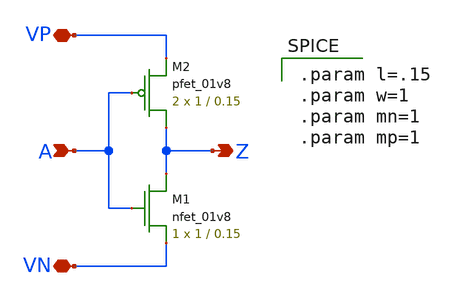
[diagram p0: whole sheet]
** sch_path: schematics/inverter.sch
**.subckt inverter A VP VN Z
*.ipin A
*.iopin VP
*.iopin VN
*.opin Z
XM1 Z A VN GND sky130_fd_pr__nfet_01v8 L=0.15 W=1 nf=1 ad='int((nf+1)/2) * W/nf * 0.29' as='int((nf+2)/2) * W/nf * 0.29'
+ pd='2*int((nf+1)/2) * (W/nf + 0.29)' ps='2*int((nf+2)/2) * (W/nf + 0.29)' nrd='0.29 / W' nrs='0.29 / W'
+ sa=0 sb=0 sd=0 mult=1 m=1
XM2 Z A VP VDD sky130_fd_pr__pfet_01v8 L=0.15 W=1 nf=1 ad='int((nf+1)/2) * W/nf * 0.29' as='int((nf+2)/2) * W/nf * 0.29'
+ pd='2*int((nf+1)/2) * (W/nf + 0.29)' ps='2*int((nf+2)/2) * (W/nf + 0.29)' nrd='0.29 / W' nrs='0.29 / W'
+ sa=0 sb=0 sd=0 mult=2 m=2
**** begin user architecture code

.param l=.15
.param w=1
.param mn=1
.param mp=1

**** end user architecture code
**.ends
.end
